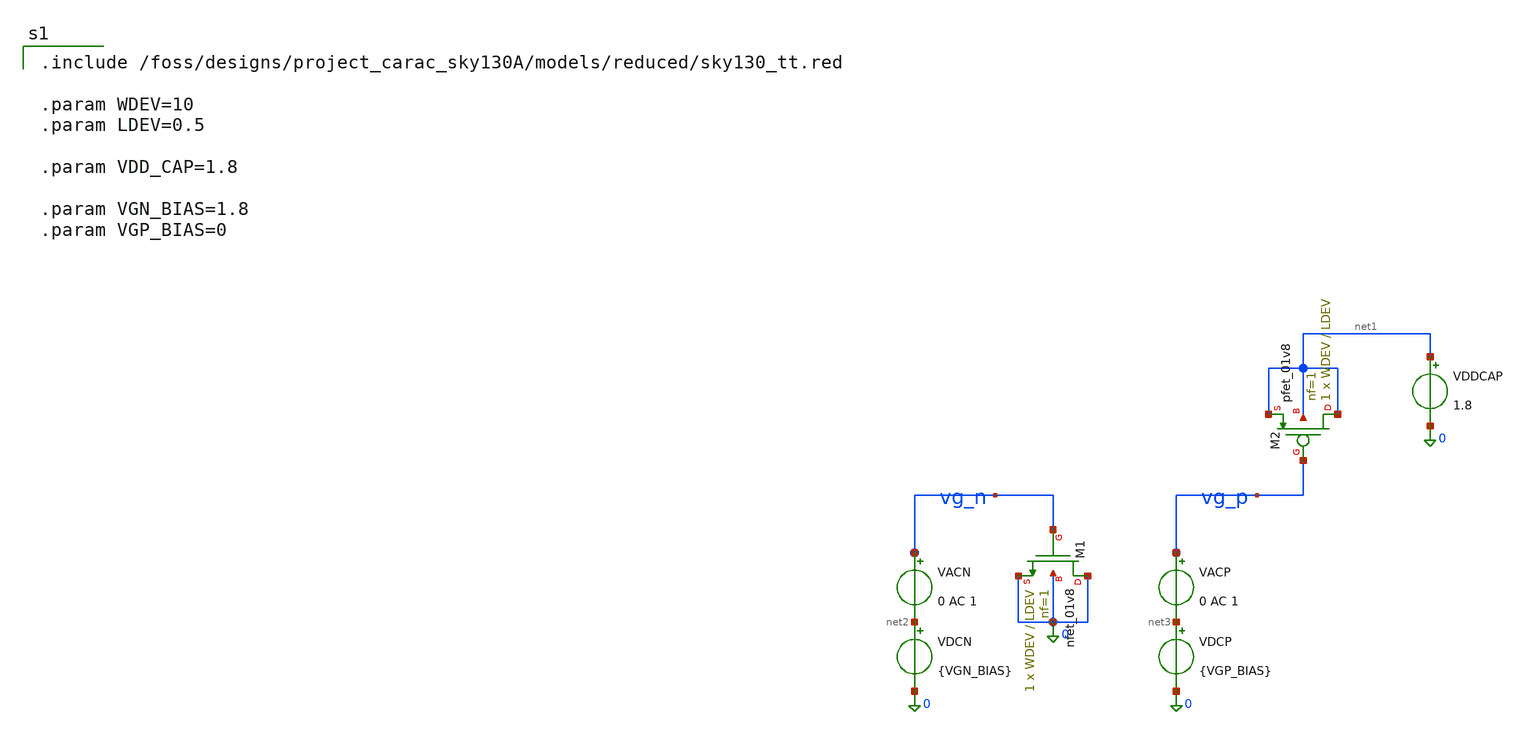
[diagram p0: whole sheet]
** sch_path: dfii/project_carac_sky130A_sim/tb_mos_01v8_moscap.sch
* Copyright 2021 Stefan Frederik Schippers
* Licensed under the Apache License, Version 2.0 (the "License");
* you may not use this file except in compliance with the License.
* You may obtain a copy of the License at
* https://www.apache.org/licenses/LICENSE-2.0
* Unless required by applicable law or agreed to in writing, software
* distributed under the License is distributed on an "AS IS" BASIS,
* WITHOUT WARRANTIES OR CONDITIONS OF ANY KIND, either express or implied.
* See the License for the specific language governing permissions and
* limitations under the License.

.include /foss/designs/project_carac_sky130A/models/reduced/sky130_tt.red

.param WDEV=10
.param LDEV=0.5

.param VDD_CAP=1.8

.param VGN_BIAS=1.8
.param VGP_BIAS=0


**.subckt tb_mos_01v8_moscap
XM1 0 vg_n 0 0 sky130_fd_pr__nfet_01v8 L=LDEV W=WDEV nf=1 ad='int((1 + 1)/2) * WDEV / 1 * 0.29' as='int((1 + 2)/2) * WDEV / 1 * 0.29'
+ pd='2*int((1 + 1)/2) * (WDEV / 1 + 0.29)' ps='2*int((1 + 2)/2) * (WDEV / 1 + 0.29)' nrd='0.29 / WDEV '
+ nrs='0.29 / WDEV ' sa=0 sb=0 sd=0 mult=1 m=1
VACN vg_n net2 0 AC 1
VDCN net2 0 {VGN_BIAS}
VACP vg_p net3 0 AC 1
VDCP net3 0 {VGP_BIAS}
XM2 net1 vg_p net1 net1 sky130_fd_pr__pfet_01v8 L=LDEV W=WDEV nf=1 ad='int((1 + 1)/2) * WDEV / 1 * 0.29'
+ as='int((1 + 2)/2) * WDEV / 1 * 0.29' pd='2*int((1 + 1)/2) * (WDEV / 1 + 0.29)' ps='2*int((1 + 2)/2) * (WDEV / 1 + 0.29)'
+ nrd='0.29 / WDEV ' nrs='0.29 / WDEV ' sa=0 sb=0 sd=0 mult=1 m=1
VDDCAP net1 0 1.8
**.ends
**** begin user architecture code

.control

* ============================================================
* A) Cg versus gate potential
* Reference geometry: W=10um, L=0.5um
* D=S=B=0
* ============================================================

* ============================================================
* A) Cg versus capacitor voltage
* Reference geometry: W=10um, L=0.5um
* ============================================================

setplot const

let k = 0
let npts = 36
let vcap_step = 0.05

echo Vcap_V Cg_N_F Cg_P_F > tb_mos_01v8_moscap_cv.dat

while k le npts

    let vcap_val = k * vcap_step
    let vgp_val  = 1.8 - vcap_val

    alter VDCN $&vcap_val
    alter VDCP $&vgp_val

    ac lin 1 1Meg 1Meg

    let cgn_now = abs(imag(i(VACN))) / (2*pi*frequency)
    let cgp_now = abs(imag(i(VACP))) / (2*pi*frequency)

    echo $&vcap_val $&cgn_now $&cgp_now >> tb_mos_01v8_moscap_cv.dat

    setplot const
    let k = k + 1

end


* ============================================================
* B) Cg versus geometry
* Fixed capacitor bias: VGB = 1.8V
* ============================================================

* ============================================================
* B) Cg versus geometry
* Fixed |VGB| = 1.8V
* ============================================================

setplot const

let w_val   = 1
let w_stop  = 20
let w_step  = 1

let l_start = 0.5
let l_stop  = 10
let l_step  = 0.5

echo W_um L_um Cg_N_F Cg_Ndens_fF_um2 Cg_P_F Cg_Pdens_fF_um2 > tb_mos_01v8_moscap_geometry.dat

while w_val le w_stop

    let l_val = l_start

    while l_val le l_stop

        alterparam WDEV = $&w_val
        alterparam LDEV = $&l_val

        reset

        ac lin 1 1Meg 1Meg

        let cgn_now = abs(imag(i(VACN))) / (2*pi*frequency)
        let cgp_now = abs(imag(i(VACP))) / (2*pi*frequency)

        let cgn_density = cgn_now*1e15 / ($&w_val*$&l_val)
        let cgp_density = cgp_now*1e15 / ($&w_val*$&l_val)

        echo $&w_val $&l_val $&cgn_now $&cgn_density $&cgp_now $&cgp_density >>
+ tb_mos_01v8_moscap_geometry.dat

        setplot const
        let l_val = l_val + l_step

    end

    let w_val = w_val + w_step

end

.endc

**** end user architecture code
.end
